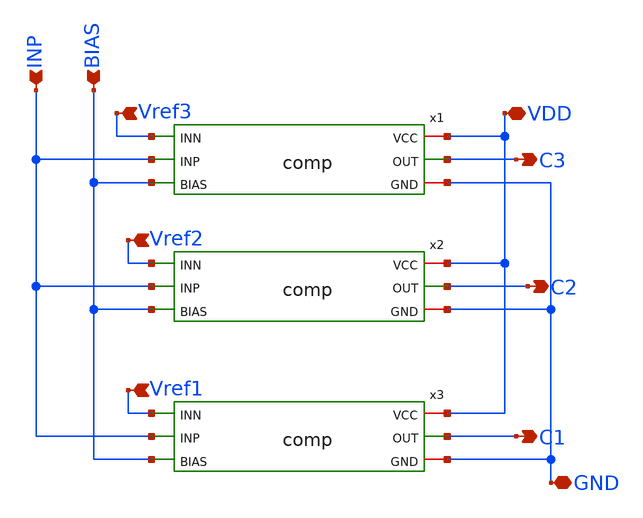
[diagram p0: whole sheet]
** sch_path: week7/pre-layout/sp_twobit.sch
**.subckt sp_twobit GND VDD C3 C2 C1 Vref2 Vref3 Vref1 BIAS INP
*.iopin GND
*.iopin VDD
*.opin C3
*.opin C2
*.opin C1
*.ipin Vref2
*.ipin Vref3
*.ipin Vref1
*.ipin BIAS
*.ipin INP
x1 VDD C3 Vref3 INP GND BIAS comp
x2 VDD C2 Vref2 INP GND BIAS comp
x3 VDD C1 Vref1 INP GND BIAS comp
**.ends

* expanding   symbol:  comp.sym # of pins=6
** sym_path: week7/pre-layout/comp.sym
** sch_path: week7/pre-layout/comp.sch
.subckt comp VCC OUT INN INP GND BIAS
*.ipin BIAS
*.iopin VCC
*.iopin GND
*.opin OUT
*.ipin INN
*.ipin INP
XM1 net3 net3 VCC VCC sky130_fd_pr__pfet_01v8 L=0.15 W=0.84 nf=1 ad='int((nf+1)/2) * W/nf * 0.29' as='int((nf+2)/2) * W/nf * 0.29'
+ pd='2*int((nf+1)/2) * (W/nf + 0.29)' ps='2*int((nf+2)/2) * (W/nf + 0.29)' nrd='0.29 / W' nrs='0.29 / W'
+ sa=0 sb=0 sd=0 mult=1 m=1
XM3 net3 INN net1 GND sky130_fd_pr__nfet_01v8 L=0.15 W=0.84 nf=1 ad='int((nf+1)/2) * W/nf * 0.29' as='int((nf+2)/2) * W/nf * 0.29'
+ pd='2*int((nf+1)/2) * (W/nf + 0.29)' ps='2*int((nf+2)/2) * (W/nf + 0.29)' nrd='0.29 / W' nrs='0.29 / W'
+ sa=0 sb=0 sd=0 mult=1 m=1
XM12 net1 BIAS GND GND sky130_fd_pr__nfet_01v8 L=0.15 W=0.84 nf=1 ad='int((nf+1)/2) * W/nf * 0.29' as='int((nf+2)/2) * W/nf * 0.29'
+ pd='2*int((nf+1)/2) * (W/nf + 0.29)' ps='2*int((nf+2)/2) * (W/nf + 0.29)' nrd='0.29 / W' nrs='0.29 / W'
+ sa=0 sb=0 sd=0 mult=1 m=1
XM2 net2 net3 VCC VCC sky130_fd_pr__pfet_01v8 L=0.15 W=0.84 nf=1 ad='int((nf+1)/2) * W/nf * 0.29' as='int((nf+2)/2) * W/nf * 0.29'
+ pd='2*int((nf+1)/2) * (W/nf + 0.29)' ps='2*int((nf+2)/2) * (W/nf + 0.29)' nrd='0.29 / W' nrs='0.29 / W'
+ sa=0 sb=0 sd=0 mult=1 m=1
XM4 net2 INP net1 GND sky130_fd_pr__nfet_01v8 L=0.15 W=0.84 nf=1 ad='int((nf+1)/2) * W/nf * 0.29' as='int((nf+2)/2) * W/nf * 0.29'
+ pd='2*int((nf+1)/2) * (W/nf + 0.29)' ps='2*int((nf+2)/2) * (W/nf + 0.29)' nrd='0.29 / W' nrs='0.29 / W'
+ sa=0 sb=0 sd=0 mult=1 m=1
XM5 net4 net2 VCC VCC sky130_fd_pr__pfet_01v8 L=0.15 W=0.84 nf=1 ad='int((nf+1)/2) * W/nf * 0.29' as='int((nf+2)/2) * W/nf * 0.29'
+ pd='2*int((nf+1)/2) * (W/nf + 0.29)' ps='2*int((nf+2)/2) * (W/nf + 0.29)' nrd='0.29 / W' nrs='0.29 / W'
+ sa=0 sb=0 sd=0 mult=1 m=1
XM6 net4 net2 GND GND sky130_fd_pr__nfet_01v8 L=0.15 W=0.84 nf=1 ad='int((nf+1)/2) * W/nf * 0.29' as='int((nf+2)/2) * W/nf * 0.29'
+ pd='2*int((nf+1)/2) * (W/nf + 0.29)' ps='2*int((nf+2)/2) * (W/nf + 0.29)' nrd='0.29 / W' nrs='0.29 / W'
+ sa=0 sb=0 sd=0 mult=1 m=1
XM7 net5 net4 GND GND sky130_fd_pr__nfet_01v8 L=0.15 W=0.84 nf=1 ad='int((nf+1)/2) * W/nf * 0.29' as='int((nf+2)/2) * W/nf * 0.29'
+ pd='2*int((nf+1)/2) * (W/nf + 0.29)' ps='2*int((nf+2)/2) * (W/nf + 0.29)' nrd='0.29 / W' nrs='0.29 / W'
+ sa=0 sb=0 sd=0 mult=1 m=1
XM8 OUT net5 GND GND sky130_fd_pr__nfet_01v8 L=0.15 W=0.84 nf=1 ad='int((nf+1)/2) * W/nf * 0.29' as='int((nf+2)/2) * W/nf * 0.29'
+ pd='2*int((nf+1)/2) * (W/nf + 0.29)' ps='2*int((nf+2)/2) * (W/nf + 0.29)' nrd='0.29 / W' nrs='0.29 / W'
+ sa=0 sb=0 sd=0 mult=1 m=1
XM9 net5 net4 VCC VCC sky130_fd_pr__pfet_01v8 L=0.15 W=0.84 nf=1 ad='int((nf+1)/2) * W/nf * 0.29' as='int((nf+2)/2) * W/nf * 0.29'
+ pd='2*int((nf+1)/2) * (W/nf + 0.29)' ps='2*int((nf+2)/2) * (W/nf + 0.29)' nrd='0.29 / W' nrs='0.29 / W'
+ sa=0 sb=0 sd=0 mult=1 m=1
XM10 OUT net5 VCC VCC sky130_fd_pr__pfet_01v8 L=0.15 W=0.84 nf=1 ad='int((nf+1)/2) * W/nf * 0.29' as='int((nf+2)/2) * W/nf * 0.29'
+ pd='2*int((nf+1)/2) * (W/nf + 0.29)' ps='2*int((nf+2)/2) * (W/nf + 0.29)' nrd='0.29 / W' nrs='0.29 / W'
+ sa=0 sb=0 sd=0 mult=1 m=1
.ends

.end
